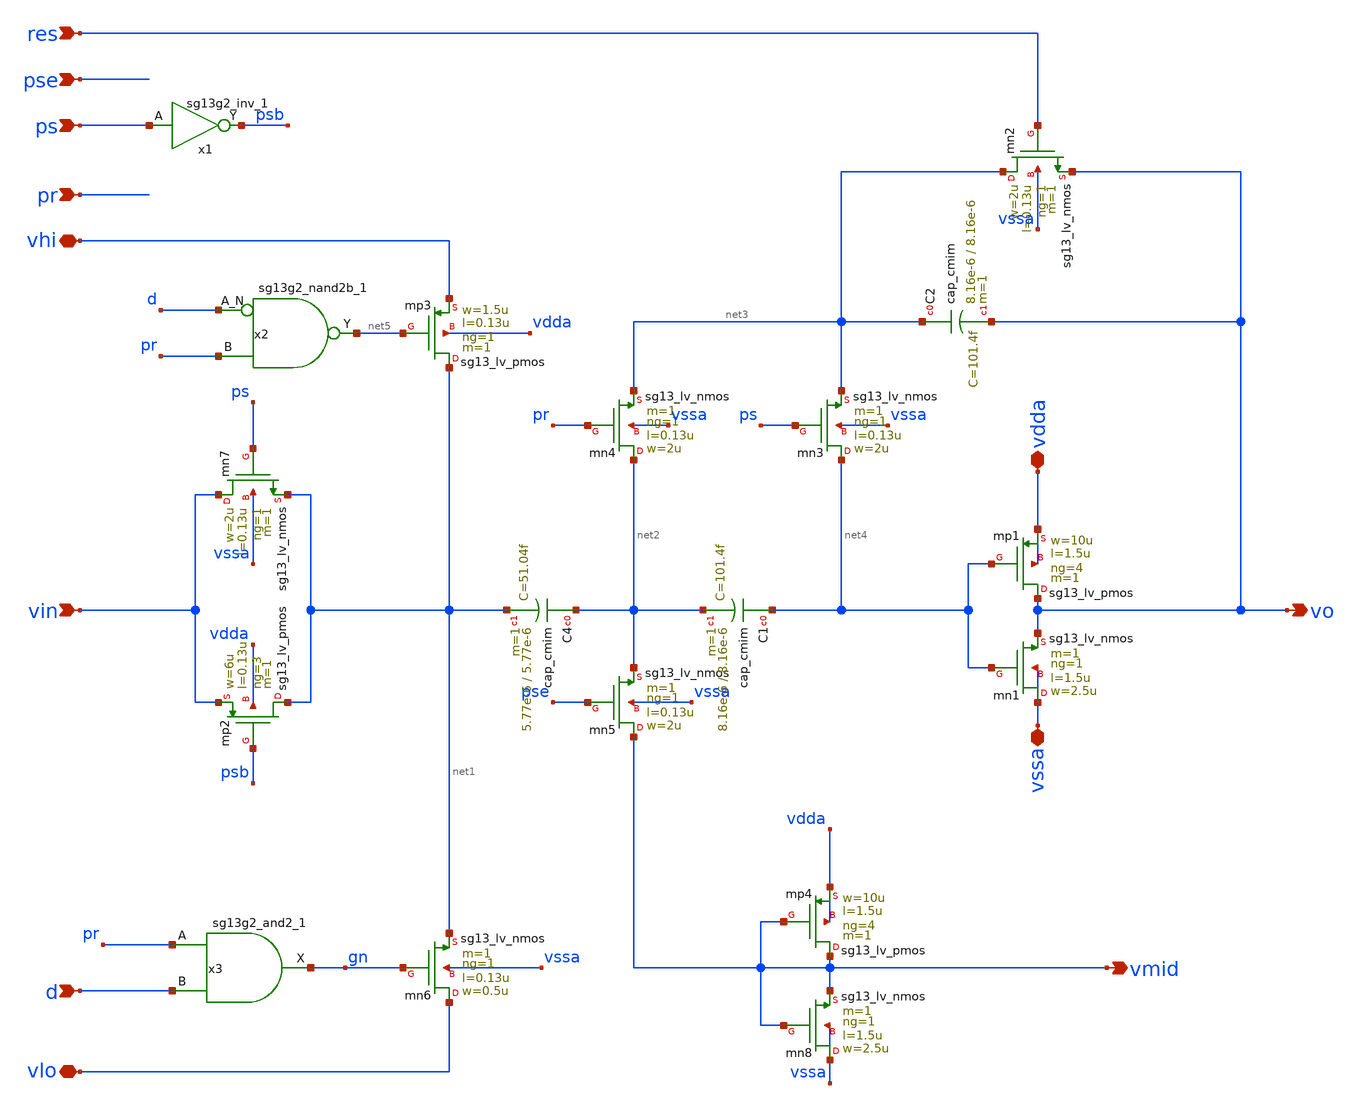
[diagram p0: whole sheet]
** sch_path: 5_Design/4_Layout/Team 3/xschem/stage_Team3.sch
* IHP-GmbH/IHP-Open-PDK/ihp-sg13g2/libs.tech/xschem/sg13g2_stdcells/sg13g2_nand2b_1.sch:
* Copyright 2023 IHP PDK Authors
* Licensed under the Apache License, Version 2.0 (the "License");
**.subckt stage_Team3 res pse ps pr vin vdda vo vssa vhi d vlo vmid
*.ipin res
*.ipin pse
*.ipin ps
*.ipin pr
*.ipin vin
*.iopin vdda
*.opin vo
*.iopin vssa
*.iopin vhi
*.ipin d
*.iopin vlo
*.opin vmid
Xmn1 vssa net4 vo vssa sg13_lv_nmos w=2.5u l=1.5u ng=1 m=1 mm_ok=1
Xmp1 vo net4 vdda vdda sg13_lv_pmos w=10u l=1.5u ng=4 m=1 mm_ok=1
Xmn2 net3 res vo vssa sg13_lv_nmos w=2u l=0.13u ng=1 m=1 mm_ok=1
Xmn3 net4 ps net3 vssa sg13_lv_nmos w=2u l=0.13u ng=1 m=1 mm_ok=1
Xmn4 net2 pr net3 vssa sg13_lv_nmos w=2u l=0.13u ng=1 m=1 mm_ok=1
Xmn5 vmid pse net2 vssa sg13_lv_nmos w=2u l=0.13u ng=1 m=1 mm_ok=1
Xmp2 net1 psb vin vdda sg13_lv_pmos w=6u l=0.13u ng=3 m=1 mm_ok=1
Xmn6 vlo gn net1 vssa sg13_lv_nmos w=0.5u l=0.13u ng=1 m=1 mm_ok=1
Xmn7 vin ps net1 vssa sg13_lv_nmos w=2u l=0.13u ng=1 m=1 mm_ok=1
x1 psb ps VDD VSS sg13g2_inv_1
Xmp3 net1 net5 vhi vdda sg13_lv_pmos w=1.5u l=0.13u ng=1 m=1 mm_ok=1
x3 gn pr d VDD VSS sg13g2_and2_1
Xmn8 vssa vmid vmid vssa sg13_lv_nmos w=2.5u l=1.5u ng=1 m=1 mm_ok=1
Xmp4 vmid vmid vdda vdda sg13_lv_pmos w=10u l=1.5u ng=4 m=1 mm_ok=1
XC4 net2 net1 cap_cmim w=5.77e-6 l=5.77e-6 m=1 mm_ok=1
XC1 net4 net2 cap_cmim w=8.16e-6 l=8.16e-6 m=1 mm_ok=1
XC2 net3 vo cap_cmim w=8.16e-6 l=8.16e-6 m=1 mm_ok=1
x2 net5 d pr VDD VSS sg13g2_nand2b_1
**.ends

* expanding   symbol:  sg13g2_stdcells/sg13g2_inv_1.sym # of pins=2
** sym_path: sg13g2_stdcells/sg13g2_inv_1.sym
** sch_path: sg13g2_stdcells/sg13g2_inv_1.sch
.subckt sg13g2_inv_1 Y A VDD VSS
*.opin Y
*.ipin A
*.iopin VDD
*.iopin VSS
XM1 Y A VSS VSS sg13_lv_nmos w=740.00n l=130.00n ng=1 m=1 mm_ok=1
XM2 Y A VDD VDD sg13_lv_pmos w=1.12u l=130.00n ng=1 m=1 mm_ok=1
.ends


* expanding   symbol:  sg13g2_stdcells/sg13g2_and2_1.sym # of pins=3
** sym_path: sg13g2_stdcells/sg13g2_and2_1.sym
** sch_path: sg13g2_stdcells/sg13g2_and2_1.sch
.subckt sg13g2_and2_1 X A B VDD VSS
*.ipin A
*.ipin B
*.opin X
*.iopin VDD
*.iopin VSS
XM1 net1 A net2 VSS sg13_lv_nmos w=640.00n l=130.00n ng=1 m=1 mm_ok=1
XM2 net2 B VSS VSS sg13_lv_nmos w=640.00n l=130.00n ng=1 m=1 mm_ok=1
XM3 X net1 VSS VSS sg13_lv_nmos w=740.00n l=130.00n ng=1 m=1 mm_ok=1
XM4 net1 B VDD VDD sg13_lv_pmos w=840.00n l=130.00n ng=1 m=1 mm_ok=1
XM5 net1 A VDD VDD sg13_lv_pmos w=840.00n l=130.00n ng=1 m=1 mm_ok=1
XM6 X net1 VDD VDD sg13_lv_pmos w=1.12u l=130.00n ng=1 m=1 mm_ok=1
.ends


* expanding   symbol:  sg13g2_stdcells/sg13g2_nand2b_1.sym # of pins=3
** sym_path: sg13g2_stdcells/sg13g2_nand2b_1.sym
** sch_path: sg13g2_stdcells/sg13g2_nand2b_1.sch
.subckt sg13g2_nand2b_1 Y A_N B VDD VSS
*.opin Y
*.ipin B
*.ipin A_N
*.iopin VDD
*.iopin VSS
XM1 net1 A_N VSS VSS sg13_lv_nmos w=550.00n l=130.00n ng=1 m=1 mm_ok=1
XM2 Y net1 net2 VSS sg13_lv_nmos w=740.00n l=130.00n ng=1 m=1 mm_ok=1
XM3 net2 B VSS VSS sg13_lv_nmos w=740.00n l=130.00n ng=1 m=1 mm_ok=1
XM4 Y B VDD VDD sg13_lv_pmos w=1.12u l=130.00n ng=1 m=1 mm_ok=1
XM5 net1 A_N VDD VDD sg13_lv_pmos w=840.00n l=130.00n ng=1 m=1 mm_ok=1
XM6 Y net1 VDD VDD sg13_lv_pmos w=1.12u l=130.00n ng=1 m=1 mm_ok=1
.ends

.end
